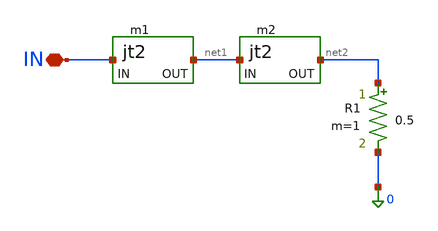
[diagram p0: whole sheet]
** sch_path: cells/stdload.sch
**.subckt stdload IN
*.iopin IN
Xm1 IN net1 jt2
R1 net2 0 0.5 m=1
Xm2 net1 net2 jt2
**.ends

* expanding   symbol:  jt2.sym # of pins=2
** sym_path: cells/jt2.sym
** sch_path: cells/jt2.sch
.subckt jt2 IN OUT
*.iopin OUT
*.iopin IN
L1 net3 net2 0.75 m=1
L2 net2 net1 0.75 m=1
I0 0 net2 I?
L5 net1 IN 0.75 m=1
L6 OUT net3 0.75 m=1
J1 net1 0 J
J2 net3 0 J
.ends

.end
